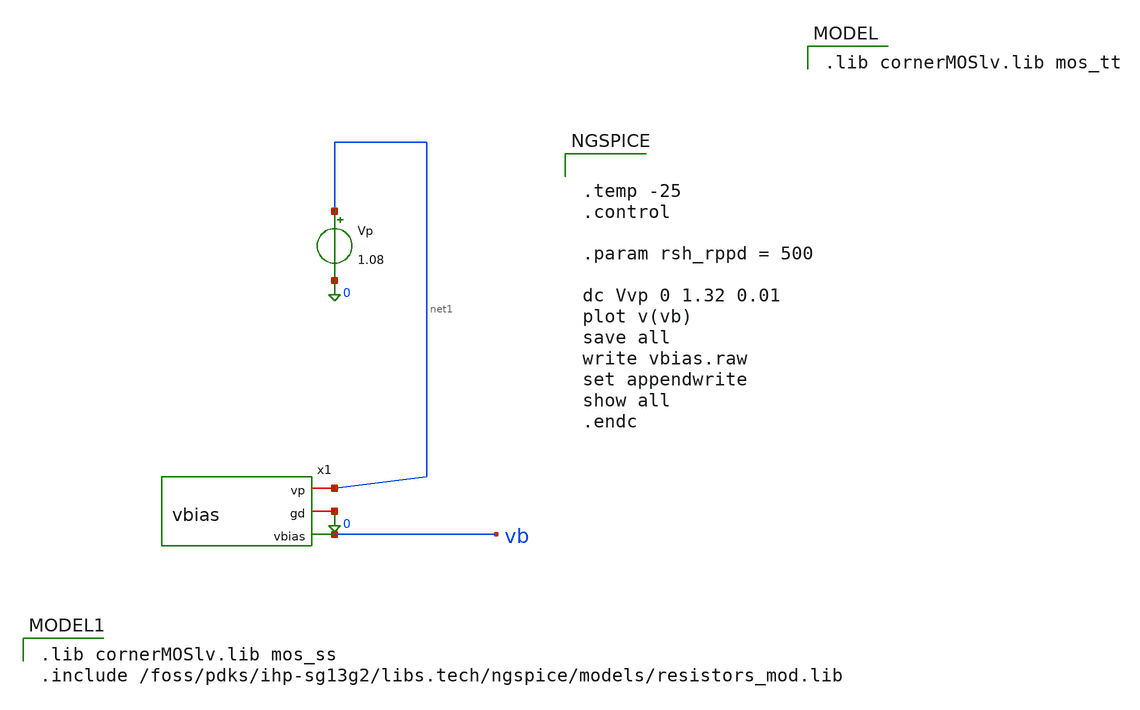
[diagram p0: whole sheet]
** sch_path: charge_pump/vbias_tb.sch
**.subckt vbias_tb
Vp net1 0 1.08
x1 net1 0 vb vbias
**** begin user architecture code
 .lib cornerMOSlv.lib mos_tt



.temp -25
.control

.param rsh_rppd = 500

dc Vvp 0 1.32 0.01
plot v(vb)
save all
write vbias.raw
set appendwrite
show all
.endc


 .lib cornerMOSlv.lib mos_ss
.include /foss/pdks/ihp-sg13g2/libs.tech/ngspice/models/resistors_mod.lib

**** end user architecture code
**.ends

* expanding   symbol:  /foss/designs/CHIP-PLL/charge_pump/vbias.sym # of pins=3
** sym_path: schematics/charge_pump/vbias.sym
** sch_path: schematics/charge_pump/vbias.sch
.subckt vbias vp gd vbias
*.opin vbias
*.iopin gd
*.iopin vp
XM5 net1 iref vp vp sg13_lv_pmos w=1.2u l=0.6u ng=1 m=1 mm_ok=1
XM6 vbias net1 net2 gd sg13_lv_nmos w=3.6u l=0.6u ng=1 m=1 mm_ok=1
XM2 net2 net2 gd gd sg13_lv_nmos w=1.2u l=0.6u ng=1 m=1 mm_ok=1
XM3 gd gd gd gd sg13_lv_nmos w=1.86u l=0.6u ng=1 m=1 mm_ok=1
XM7 vp vp vp vp sg13_lv_pmos w=1.375u l=0.6u ng=1 m=1 mm_ok=1
XR1 net1 vbias gd rppd w=1e-6 l=1.7e-6 m=1 b=0 mm_ok=1
x1 vp iref gd curr_source
.ends


* expanding   symbol:  /foss/designs/CHIP-PLL/schematics/charge_pump/curr_source.sym # of pins=3
** sym_path: charge_pump/curr_source.sym
** sch_path: charge_pump/curr_source.sch
.subckt curr_source vp iref gd
*.iopin vp
*.iopin gd
*.opin iref
XM4 iref iref vp vp sg13_lv_pmos w=1.4u l=0.6u ng=1 m=1 mm_ok=1
XM5 net2 iref vp vp sg13_lv_pmos w=1.2u l=0.6u ng=1 m=1 mm_ok=1
XM6 net3 net3 gd gd sg13_lv_nmos w=1u l=0.6u ng=1 m=1 mm_ok=1
XM3 net2 net2 gd gd sg13_lv_nmos w=1.4u l=0.6u ng=1 m=1 mm_ok=1
XR2 net1 gd gd rppd w=1e-6 l=1.70e-6 m=1 b=0 mm_ok=1
XM1 iref net2 net1 gd sg13_lv_nmos w=1.2u l=0.6u ng=1 m=1 mm_ok=1
XM2 vp net3 iref gd sg13_lv_nmos w=1u l=0.6u ng=1 m=1 mm_ok=1
XM7 vp vp net3 gd sg13_lv_nmos w=1u l=0.6u ng=1 m=1 mm_ok=1
XM8 gd gd gd gd sg13_lv_nmos w=0.4u l=0.6u ng=1 m=1 mm_ok=1
.ends

.end
